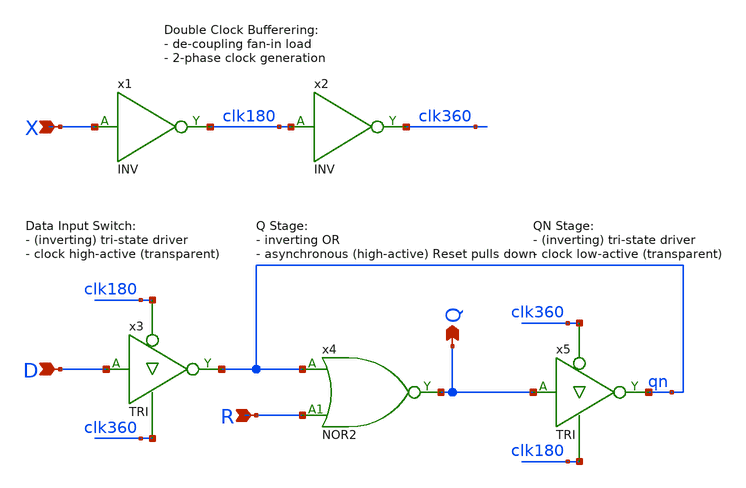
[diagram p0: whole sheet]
** sch_path: Sources/crafted/LATPR.sch
**.subckt LATPR X D Q R
*.ipin X
*.ipin D
*.opin Q
*.ipin R
x3 D clk180 clk360 qn VDD GND TRI Wmin=1.5u Lmin=1u g=2 m=1
x5 Q clk360 clk180 qn VDD GND TRI Wmin=1.5u Lmin=1u g=2 m=1
x4 qn R Q VDD GND NOR2 Wmin=1.5u Lmin=1u g=2 m=1
x1 X clk180 VDD GND INV Wmin=1.5u Lmin=1u g=2 m=1
x2 clk180 clk360 VDD GND INV Wmin=1.5u Lmin=1u g=2 m=1
**.ends
.end
